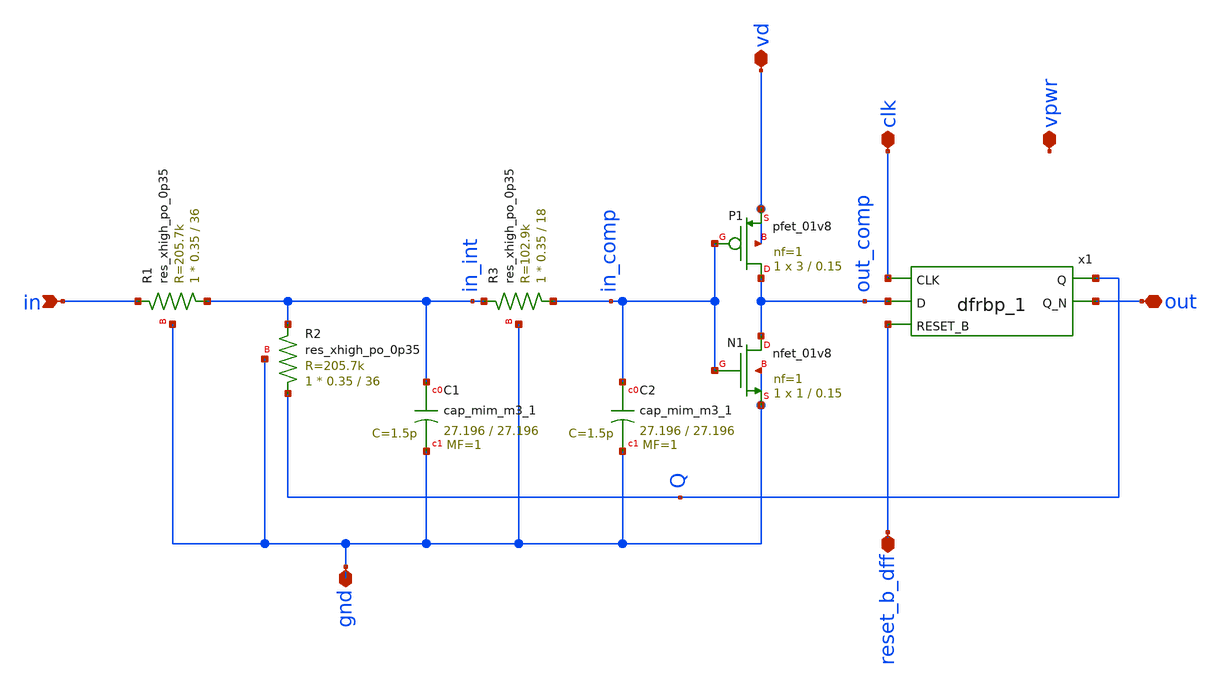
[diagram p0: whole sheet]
** sch_path: mag/sigma-delta_modulator/xschem/sigma-delta.sch
* Copyright 2020 Stefan Frederik Schippers
* Licensed under the Apache License, Version 2.0 (the "License");
* you may not use this file except in compliance with the License.
* You may obtain a copy of the License at
* https://www.apache.org/licenses/LICENSE-2.0
* Unless required by applicable law or agreed to in writing, software
* distributed under the License is distributed on an "AS IS" BASIS,
* WITHOUT WARRANTIES OR CONDITIONS OF ANY KIND, either express or implied.
* See the License for the specific language governing permissions and
* limitations under the License.
**.subckt sigma-delta in gnd clk out reset_b_dff vpwr vd
*.ipin in
*.iopin gnd
*.iopin clk
*.iopin out
*.iopin reset_b_dff
*.iopin vpwr
*.iopin vd
XR2 Q in_int gnd sky130_fd_pr__res_xhigh_po_0p35 L=36 mult=1 m=1
XR1 in_int in gnd sky130_fd_pr__res_xhigh_po_0p35 L=36 mult=1 m=1
XN1 out_comp in_comp gnd gnd sky130_fd_pr__nfet_01v8 L=0.15 W=1 nf=1 ad='int((nf+1)/2) * W/nf * 0.29'
+ as='int((nf+2)/2) * W/nf * 0.29' pd='2*int((nf+1)/2) * (W/nf + 0.29)' ps='2*int((nf+2)/2) * (W/nf + 0.29)'
+ nrd='0.29 / W' nrs='0.29 / W' sa=0 sb=0 sd=0 mult=1 m=1
XP1 out_comp in_comp vd vd sky130_fd_pr__pfet_01v8 L=0.15 W=3 nf=1 ad='int((nf+1)/2) * W/nf * 0.29' as='int((nf+2)/2) * W/nf * 0.29'
+ pd='2*int((nf+1)/2) * (W/nf + 0.29)' ps='2*int((nf+2)/2) * (W/nf + 0.29)' nrd='0.29 / W' nrs='0.29 / W'
+ sa=0 sb=0 sd=0 mult=1 m=1
x1 clk out_comp reset_b_dff GND GND VPWR VPWR Q out sky130_fd_sc_hd__dfrbp_1
XR3 in_comp in_int gnd sky130_fd_pr__res_xhigh_po_0p35 L=18 mult=1 m=1
XC1 in_int gnd sky130_fd_pr__cap_mim_m3_1 W=27.196 L=27.196 MF=1 m=1
XC2 in_comp gnd sky130_fd_pr__cap_mim_m3_1 W=27.196 L=27.196 MF=1 m=1
**** begin user architecture code

.include /foss/pdks/sky130A/libs.ref/sky130_fd_sc_hd/spice/sky130_fd_sc_hd.spice


**** end user architecture code
**.ends
.end
